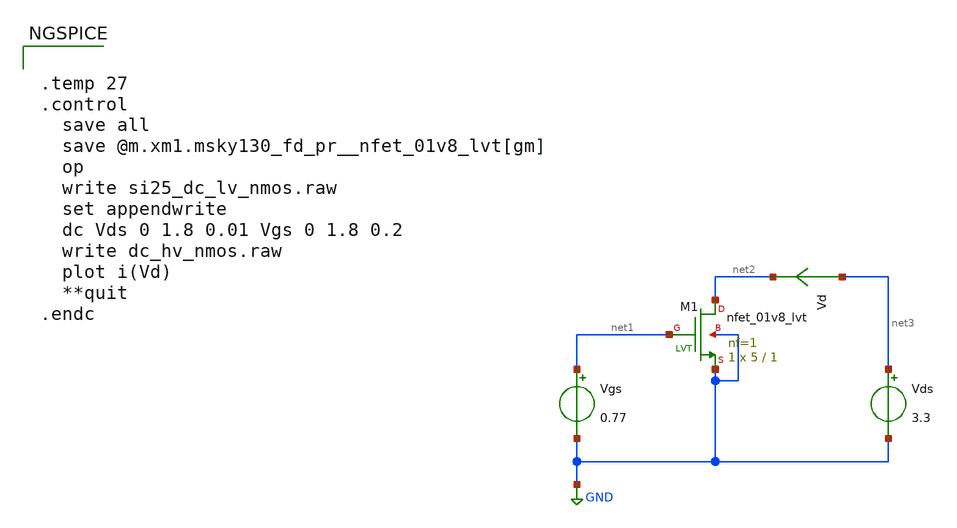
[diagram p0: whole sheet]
** sch_path: xschem/si25-dc-lv-nmos.sch
**.subckt si25-dc-lv-nmos
XM1 net2 net1 GND GND sky130_fd_pr__nfet_01v8_lvt L=1 W=5 nf=1 ad='int((1 + 1)/2) * 5 / 1 * 0.29' as='int((1 + 2)/2) * 5 / 1 * 0.29'
+ pd='2*int((1 + 1)/2) * (5 / 1 + 0.29)' ps='2*int((1 + 2)/2) * (5 / 1 + 0.29)' nrd='0.29 / 5 ' nrs='0.29 / 5 '
+ sa=0 sb=0 sd=0 mult=1 m=1
Vgs net1 GND 0.77
Vds net3 GND 3.3
Vd net3 net2 0
.save i(vd)
**** begin user architecture code


.temp 27
.control
  save all
  save @m.xm1.msky130_fd_pr__nfet_01v8_lvt[gm]
  op
  write si25_dc_lv_nmos.raw
  set appendwrite
  dc Vds 0 1.8 0.01 Vgs 0 1.8 0.2
  write dc_hv_nmos.raw
  plot i(Vd)
  **quit
.endc



** opencircuitdesign pdks install
.lib $::SKYWATER_MODELS/sky130.lib.spice tt

**** end user architecture code
**.ends
.GLOBAL GND
.end
